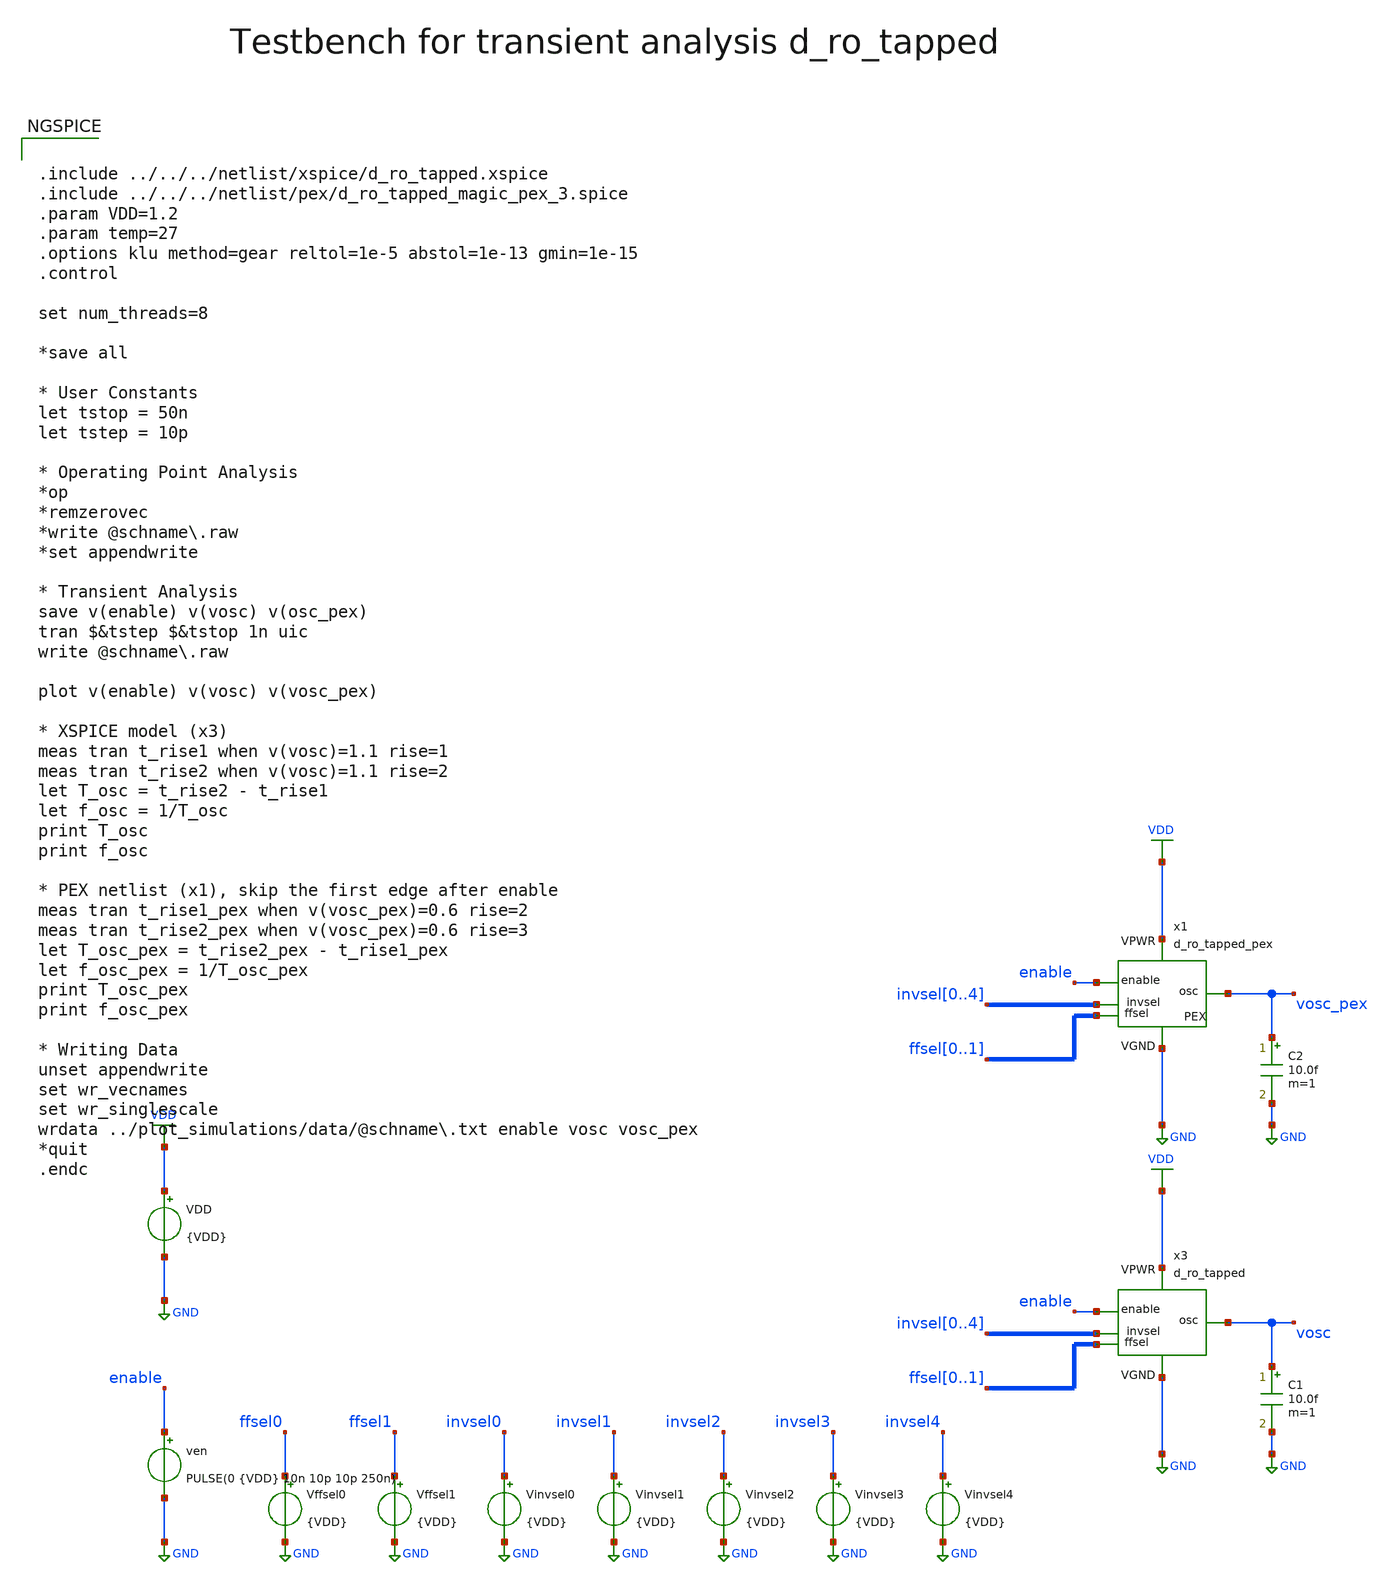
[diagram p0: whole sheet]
** sch_path: macros/heichips26_digital_project/macros/d_ro_tapped/testbenches/xschem/d_ro_tapped_tb_tran.sch
**.subckt d_ro_tapped_tb_tran
VDD VDD GND {VDD}
ven enable GND PULSE(0 {VDD} 10n 10p 10p 250n)
x1 VDD GND enable vosc_pex ffsel0 ffsel1 invsel0 invsel1 invsel2 invsel3 invsel4 d_ro_tapped_pex
C1 vosc GND 10.0f m=1
x3 VDD GND enable vosc ffsel0 ffsel1 invsel0 invsel1 invsel2 invsel3 invsel4 d_ro_tapped
Vffsel0 ffsel0 GND {VDD}
Vffsel1 ffsel1 GND {VDD}
Vinvsel0 invsel0 GND {VDD}
Vinvsel1 invsel1 GND {VDD}
Vinvsel2 invsel2 GND {VDD}
Vinvsel3 invsel3 GND {VDD}
Vinvsel4 invsel4 GND {VDD}
C2 vosc_pex GND 10.0f m=1
**** begin user architecture code


.include ../../../netlist/xspice/d_ro_tapped.xspice
.include ../../../netlist/pex/d_ro_tapped_magic_pex_3.spice
.param VDD=1.2
.param temp=27
.options klu method=gear reltol=1e-5 abstol=1e-13 gmin=1e-15
.control

set num_threads=8

*save all

* User Constants
let tstop = 50n
let tstep = 10p

* Operating Point Analysis
*op
*remzerovec
*write @schname\.raw
*set appendwrite

* Transient Analysis
save v(enable) v(vosc) v(osc_pex)
tran $&tstep $&tstop 1n uic
write @schname\.raw

plot v(enable) v(vosc) v(vosc_pex)

* XSPICE model (x3)
meas tran t_rise1 when v(vosc)=1.1 rise=1
meas tran t_rise2 when v(vosc)=1.1 rise=2
let T_osc = t_rise2 - t_rise1
let f_osc = 1/T_osc
print T_osc
print f_osc

* PEX netlist (x1), skip the first edge after enable
meas tran t_rise1_pex when v(vosc_pex)=0.6 rise=2
meas tran t_rise2_pex when v(vosc_pex)=0.6 rise=3
let T_osc_pex = t_rise2_pex - t_rise1_pex
let f_osc_pex = 1/T_osc_pex
print T_osc_pex
print f_osc_pex

* Writing Data
unset appendwrite
set wr_vecnames
set wr_singlescale
wrdata ../plot_simulations/data/@schname\.txt enable vosc vosc_pex
*quit
.endc


.lib cornerMOSlv.lib mos_tt
.lib cornerMOShv.lib mos_tt
.lib cornerRES.lib res_typ
.lib cornerDIO.lib dio_tt

**** end user architecture code
**.ends
.GLOBAL GND
.GLOBAL VDD
.end
